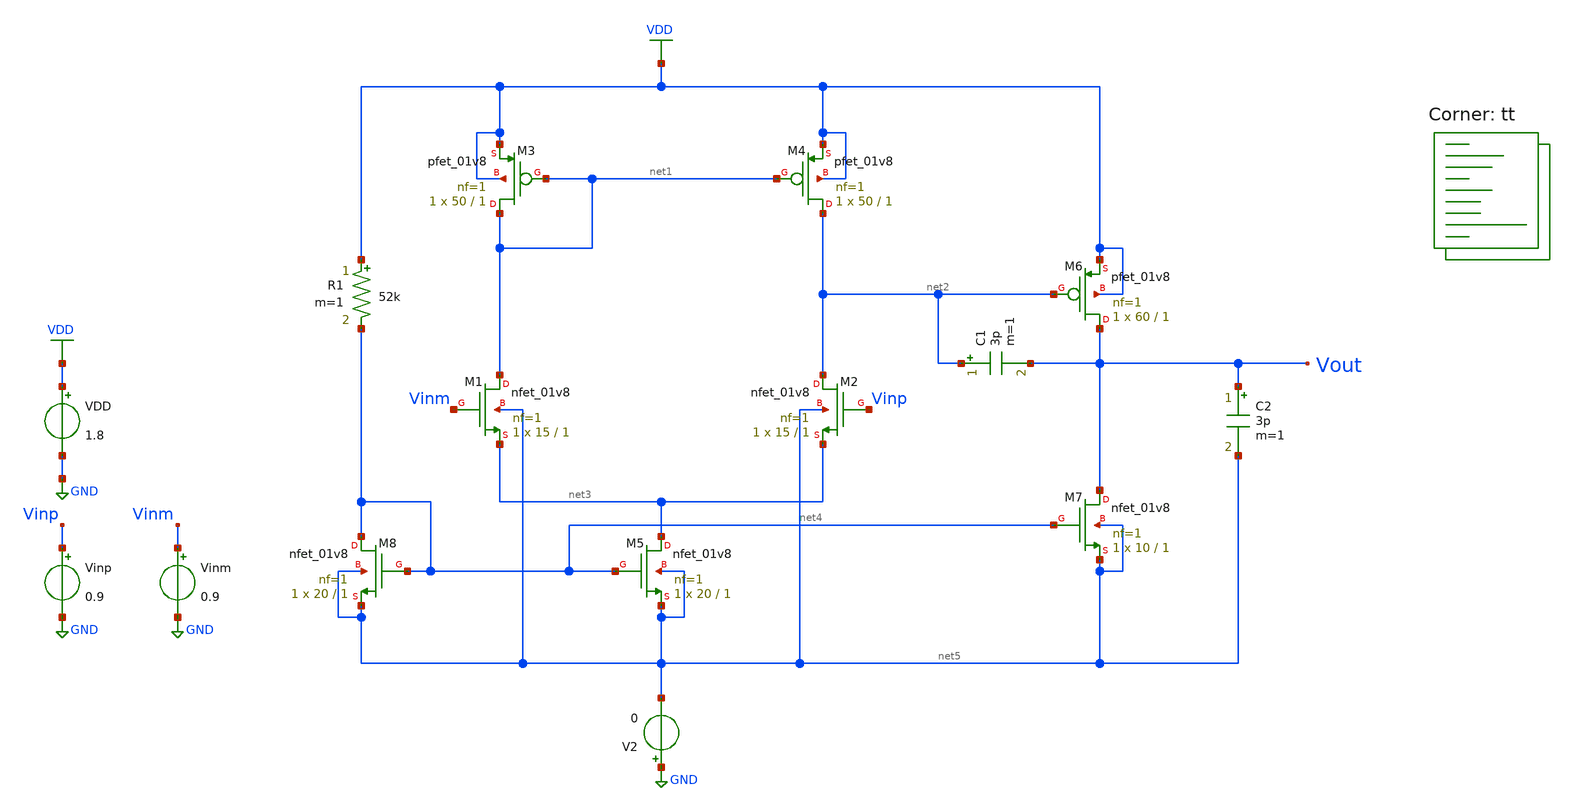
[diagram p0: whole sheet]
** sch_path: xschem/comparator_0113.sch
**.subckt comparator_0113
XM1 net1 Vinm net3 net5 sky130_fd_pr__nfet_01v8 L=1 W=15 nf=1 ad='int((1 + 1)/2) * 15 / 1 * 0.29' as='int((1 + 2)/2) * 15 / 1 * 0.29'
+ pd='2*int((1 + 1)/2) * (15 / 1 + 0.29)' ps='2*int((1 + 2)/2) * (15 / 1 + 0.29)' nrd='0.29 / 15 ' nrs='0.29 / 15 '
+ sa=0 sb=0 sd=0 mult=1 m=1
XM2 net2 Vinp net3 net5 sky130_fd_pr__nfet_01v8 L=1 W=15 nf=1 ad='int((1 + 1)/2) * 15 / 1 * 0.29' as='int((1 + 2)/2) * 15 / 1 * 0.29'
+ pd='2*int((1 + 1)/2) * (15 / 1 + 0.29)' ps='2*int((1 + 2)/2) * (15 / 1 + 0.29)' nrd='0.29 / 15 ' nrs='0.29 / 15 '
+ sa=0 sb=0 sd=0 mult=1 m=1
XM3 net1 net1 VDD VDD sky130_fd_pr__pfet_01v8 L=1 W=50 nf=1 ad='int((nf+1)/2) * W/nf * 0.29' as='int((nf+2)/2) * W/nf * 0.29'
+ pd='2*int((nf+1)/2) * (W/nf + 0.29)' ps='2*int((nf+2)/2) * (W/nf + 0.29)' nrd='0.29 / W' nrs='0.29 / W'
+ sa=0 sb=0 sd=0 mult=1 m=1
XM4 net2 net1 VDD VDD sky130_fd_pr__pfet_01v8 L=1 W=50 nf=1 ad='int((nf+1)/2) * W/nf * 0.29' as='int((nf+2)/2) * W/nf * 0.29'
+ pd='2*int((nf+1)/2) * (W/nf + 0.29)' ps='2*int((nf+2)/2) * (W/nf + 0.29)' nrd='0.29 / W' nrs='0.29 / W'
+ sa=0 sb=0 sd=0 mult=1 m=1
XM5 net3 net4 net5 net5 sky130_fd_pr__nfet_01v8 L=1 W=20 nf=1 ad='int((1 + 1)/2) * 20 / 1 * 0.29' as='int((1 + 2)/2) * 20 / 1 * 0.29'
+ pd='2*int((1 + 1)/2) * (20 / 1 + 0.29)' ps='2*int((1 + 2)/2) * (20 / 1 + 0.29)' nrd='0.29 / 20 ' nrs='0.29 / 20 '
+ sa=0 sb=0 sd=0 mult=1 m=1
XM6 Vout net2 VDD VDD sky130_fd_pr__pfet_01v8 L=1 W=60 nf=1 ad='int((nf+1)/2) * W/nf * 0.29' as='int((nf+2)/2) * W/nf * 0.29'
+ pd='2*int((nf+1)/2) * (W/nf + 0.29)' ps='2*int((nf+2)/2) * (W/nf + 0.29)' nrd='0.29 / W' nrs='0.29 / W'
+ sa=0 sb=0 sd=0 mult=1 m=1
XM7 Vout net4 net5 net5 sky130_fd_pr__nfet_01v8 L=1 W=10 nf=1 ad='int((1 + 1)/2) * 10 / 1 * 0.29' as='int((1 + 2)/2) * 10 / 1 * 0.29'
+ pd='2*int((1 + 1)/2) * (10 / 1 + 0.29)' ps='2*int((1 + 2)/2) * (10 / 1 + 0.29)' nrd='0.29 / 10 ' nrs='0.29 / 10 '
+ sa=0 sb=0 sd=0 mult=1 m=1
XM8 net4 net4 net5 net5 sky130_fd_pr__nfet_01v8 L=1 W=20 nf=1 ad='int((1 + 1)/2) * 20 / 1 * 0.29' as='int((1 + 2)/2) * 20 / 1 * 0.29'
+ pd='2*int((1 + 1)/2) * (20 / 1 + 0.29)' ps='2*int((1 + 2)/2) * (20 / 1 + 0.29)' nrd='0.29 / 20 ' nrs='0.29 / 20 '
+ sa=0 sb=0 sd=0 mult=1 m=1
R1 VDD net4 52k m=1
C1 net2 Vout 3p m=1
C2 Vout net5 3p m=1
V2 GND net5 0
VDD VDD GND 1.8
Vinp Vinp GND 0.9
Vinm Vinm GND 0.9
**** begin user architecture code
.lib $::SKYWATER_MODELS/sky130.lib.spice tt
**** end user architecture code
**.ends
.GLOBAL VDD
.GLOBAL GND
**** begin user architecture code

.options savecurrents
.control
save @m.xm1.msky130_fd_pr__nfet_01v8[vgs]
save @m.xm1.msky130_fd_pr__nfet_01v8[vds]
save @m.xm1.msky130_fd_pr__nfet_01v8[vth]
save @m.xm1.msky130_fd_pr__nfet_01v8[id]

save @m.xm2.msky130_fd_pr__nfet_01v8[vgs]
save @m.xm2.msky130_fd_pr__nfet_01v8[vds]
save @m.xm2.msky130_fd_pr__nfet_01v8[vth]
save @m.xm2.msky130_fd_pr__nfet_01v8[gm]

save @m.xm3.msky130_fd_pr__pfet_01v8[vgs]
save @m.xm3.msky130_fd_pr__pfet_01v8[vds]
save @m.xm3.msky130_fd_pr__pfet_01v8[vth]
save @m.xm3.msky130_fd_pr__pfet_01v8[gm]

save @m.xm4.msky130_fd_pr__pfet_01v8[vgs]
save @m.xm4.msky130_fd_pr__pfet_01v8[vds]
save @m.xm4.msky130_fd_pr__pfet_01v8[vth]
save @m.xm4.msky130_fd_pr__pfet_01v8[gm]

save @m.xm5.msky130_fd_pr__nfet_01v8[vgs]
save @m.xm5.msky130_fd_pr__nfet_01v8[vds]
save @m.xm5.msky130_fd_pr__nfet_01v8[vth]
save @m.xm5.msky130_fd_pr__nfet_01v8[gm]

save @m.xm6.msky130_fd_pr__pfet_01v8[vgs]
save @m.xm6.msky130_fd_pr__pfet_01v8[vds]
save @m.xm6.msky130_fd_pr__pfet_01v8[vth]
save @m.xm6.msky130_fd_pr__pfet_01v8[gm]

save @m.xm7.msky130_fd_pr__nfet_01v8[vgs]
save @m.xm7.msky130_fd_pr__nfet_01v8[vds]
save @m.xm7.msky130_fd_pr__nfet_01v8[vth]
save @m.xm1.msky130_fd_pr__nfet_01v8[gm]

save @m.xm8.msky130_fd_pr__nfet_01v8[vgs]
save @m.xm8.msky130_fd_pr__nfet_01v8[vds]
save @m.xm8.msky130_fd_pr__nfet_01v8[vth]
save @m.xm8.msky130_fd_pr__nfet_01v8[gm]

save all
op
write comparator_0113.raw
quit 0
.endc


**** end user architecture code
.end
